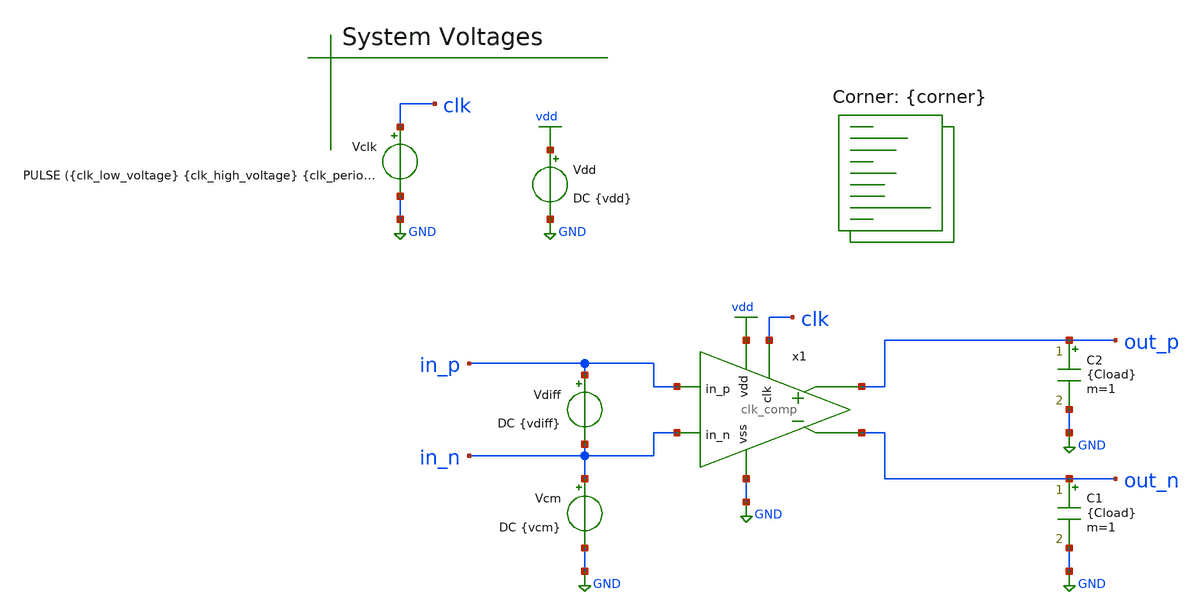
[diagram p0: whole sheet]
** sch_path: tb/tb_clk_tran.sch
**.subckt tb_clk_tran
Vdd vdd GND DC {vdd}
C1 out_n GND {Cload} m=1
Vclk clk GND PULSE ({clk_low_voltage} {clk_high_voltage} {clk_period} {clk_rise_time} {clk_fall_time}
+ '({clk_period}/2)' {clk_period} 2)
x1 vdd in_p in_n clk GND out_p out_n clk_comp
Vdiff in_p in_n DC {vdiff}
Vcm in_n GND DC {vcm}
C2 out_p GND {Cload} m=1
**** begin user architecture code


.option TEMP={temperature}
.option warn=1
.control
save clk, out_p, out_n, i(vdd)
tran {tran_step} {tran_stop} {tran_start}
let vref_data = V(clk)
wrdata {output_file} V(clk) V(out_p) V(out_n) I(vdd)
quit
.endc


.lib $::SKYWATER_MODELS/sky130.lib.spice {corner}
**** end user architecture code
**.ends

* expanding   symbol:  /home/moduhub/work/sky130_ak_ip__sigma_delta/sch/clk_comp.sym # of pins=7
** sym_path: sch/clk_comp.sym
** sch_path: sch/clk_comp.sch
.subckt clk_comp vdd in_p in_n clk vss out_p out_n
*.ipin in_p
*.ipin in_n
*.ipin vss
*.ipin vdd
*.ipin clk
*.opin out_p
*.opin out_n
XM1 net1 clk vss vss sky130_fd_pr__nfet_01v8 L=0.15 W=5 nf=1 ad='int((nf+1)/2) * W/nf * 0.29' as='int((nf+2)/2) * W/nf * 0.29'
+ pd='2*int((nf+1)/2) * (W/nf + 0.29)' ps='2*int((nf+2)/2) * (W/nf + 0.29)' nrd='0.29 / W' nrs='0.29 / W'
+ sa=0 sb=0 sd=0 mult=1 m=1
XM2 net2 in_p net1 vss sky130_fd_pr__nfet_01v8 L=1 W=5 nf=1 ad='int((nf+1)/2) * W/nf * 0.29' as='int((nf+2)/2) * W/nf * 0.29'
+ pd='2*int((nf+1)/2) * (W/nf + 0.29)' ps='2*int((nf+2)/2) * (W/nf + 0.29)' nrd='0.29 / W' nrs='0.29 / W'
+ sa=0 sb=0 sd=0 mult=1 m=1
XM3 net3 in_n net1 vss sky130_fd_pr__nfet_01v8 L=1 W=5 nf=1 ad='int((nf+1)/2) * W/nf * 0.29' as='int((nf+2)/2) * W/nf * 0.29'
+ pd='2*int((nf+1)/2) * (W/nf + 0.29)' ps='2*int((nf+2)/2) * (W/nf + 0.29)' nrd='0.29 / W' nrs='0.29 / W'
+ sa=0 sb=0 sd=0 mult=1 m=1
XM4 out_n out_p net2 vss sky130_fd_pr__nfet_01v8 L=0.15 W=2 nf=1 ad='int((nf+1)/2) * W/nf * 0.29' as='int((nf+2)/2) * W/nf * 0.29'
+ pd='2*int((nf+1)/2) * (W/nf + 0.29)' ps='2*int((nf+2)/2) * (W/nf + 0.29)' nrd='0.29 / W' nrs='0.29 / W'
+ sa=0 sb=0 sd=0 mult=1 m=1
XM5 out_p out_n net3 vss sky130_fd_pr__nfet_01v8 L=0.15 W=2 nf=1 ad='int((nf+1)/2) * W/nf * 0.29' as='int((nf+2)/2) * W/nf * 0.29'
+ pd='2*int((nf+1)/2) * (W/nf + 0.29)' ps='2*int((nf+2)/2) * (W/nf + 0.29)' nrd='0.29 / W' nrs='0.29 / W'
+ sa=0 sb=0 sd=0 mult=1 m=1
XM6 out_n clk vdd vdd sky130_fd_pr__pfet_01v8 L=0.15 W=1 nf=1 ad='int((nf+1)/2) * W/nf * 0.29' as='int((nf+2)/2) * W/nf * 0.29'
+ pd='2*int((nf+1)/2) * (W/nf + 0.29)' ps='2*int((nf+2)/2) * (W/nf + 0.29)' nrd='0.29 / W' nrs='0.29 / W'
+ sa=0 sb=0 sd=0 mult=1 m=1
XM7 out_n out_p vdd vdd sky130_fd_pr__pfet_01v8 L=0.15 W=5 nf=1 ad='int((nf+1)/2) * W/nf * 0.29' as='int((nf+2)/2) * W/nf * 0.29'
+ pd='2*int((nf+1)/2) * (W/nf + 0.29)' ps='2*int((nf+2)/2) * (W/nf + 0.29)' nrd='0.29 / W' nrs='0.29 / W'
+ sa=0 sb=0 sd=0 mult=1 m=1
XM8 out_p out_n vdd vdd sky130_fd_pr__pfet_01v8 L=0.15 W=5 nf=1 ad='int((nf+1)/2) * W/nf * 0.29' as='int((nf+2)/2) * W/nf * 0.29'
+ pd='2*int((nf+1)/2) * (W/nf + 0.29)' ps='2*int((nf+2)/2) * (W/nf + 0.29)' nrd='0.29 / W' nrs='0.29 / W'
+ sa=0 sb=0 sd=0 mult=1 m=1
XM9 out_p clk vdd vdd sky130_fd_pr__pfet_01v8 L=0.15 W=1 nf=1 ad='int((nf+1)/2) * W/nf * 0.29' as='int((nf+2)/2) * W/nf * 0.29'
+ pd='2*int((nf+1)/2) * (W/nf + 0.29)' ps='2*int((nf+2)/2) * (W/nf + 0.29)' nrd='0.29 / W' nrs='0.29 / W'
+ sa=0 sb=0 sd=0 mult=1 m=1
XM10 net2 clk vdd vdd sky130_fd_pr__pfet_01v8 L=0.15 W=1 nf=1 ad='int((nf+1)/2) * W/nf * 0.29' as='int((nf+2)/2) * W/nf * 0.29'
+ pd='2*int((nf+1)/2) * (W/nf + 0.29)' ps='2*int((nf+2)/2) * (W/nf + 0.29)' nrd='0.29 / W' nrs='0.29 / W'
+ sa=0 sb=0 sd=0 mult=1 m=1
XM11 net3 clk vdd vdd sky130_fd_pr__pfet_01v8 L=0.15 W=1 nf=1 ad='int((nf+1)/2) * W/nf * 0.29' as='int((nf+2)/2) * W/nf * 0.29'
+ pd='2*int((nf+1)/2) * (W/nf + 0.29)' ps='2*int((nf+2)/2) * (W/nf + 0.29)' nrd='0.29 / W' nrs='0.29 / W'
+ sa=0 sb=0 sd=0 mult=1 m=1
.ends

.GLOBAL vdd
.GLOBAL GND
.end
